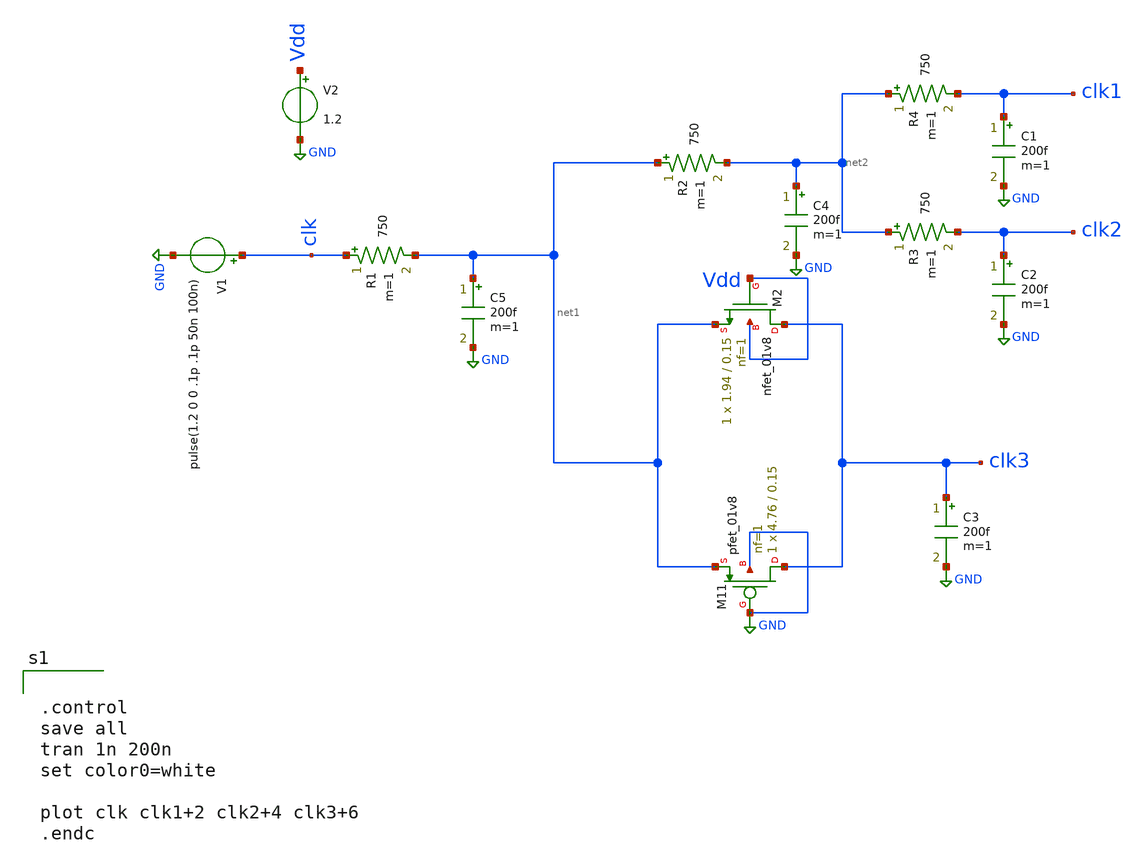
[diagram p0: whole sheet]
** sch_path: hw4/hw4.sch
**.subckt hw4
XM2 clk3 Vdd net1 Vdd sky130_fd_pr__nfet_01v8 L=0.15 W=1.94 nf=1 ad='int((1 + 1)/2) * 1.94 / 1 * 0.29'
+ as='int((1 + 2)/2) * 1.94 / 1 * 0.29' pd='2*int((1 + 1)/2) * (1.94 / 1 + 0.29)' ps='2*int((1 + 2)/2) * (1.94 / 1 + 0.29)'
+ nrd='0.29 / 1.94 ' nrs='0.29 / 1.94 ' sa=0 sb=0 sd=0 mult=1 m=1
XM11 clk3 GND net1 GND sky130_fd_pr__pfet_01v8 L=0.15 W=4.76 nf=1 ad='int((nf+1)/2) * W/nf * 0.29' as='int((nf+2)/2) * W/nf * 0.29'
+ pd='2*int((nf+1)/2) * (W/nf + 0.29)' ps='2*int((nf+2)/2) * (W/nf + 0.29)' nrd='0.29 / W' nrs='0.29 / W'
+ sa=0 sb=0 sd=0 mult=1 m=1
R1 clk net1 750 m=1
V1 clk GND pulse(1.2 0 0 .1p .1p 50n 100n)
R2 net1 net2 750 m=1
R3 net2 clk2 750 m=1
R4 net2 clk1 750 m=1
C1 clk1 GND 200f m=1
C2 clk2 GND 200f m=1
C3 clk3 GND 200f m=1
C4 net2 GND 200f m=1
C5 net1 GND 200f m=1
V2 Vdd GND 1.2
**** begin user architecture code

** opencircuitdesign pdks install
.lib $::SKYWATER_MODELS/sky130.lib.spice tt_mm




.control
save all
tran 1n 200n
set color0=white

plot clk clk1+2 clk2+4 clk3+6
.endc


**** end user architecture code
**.ends
.GLOBAL GND
.end
